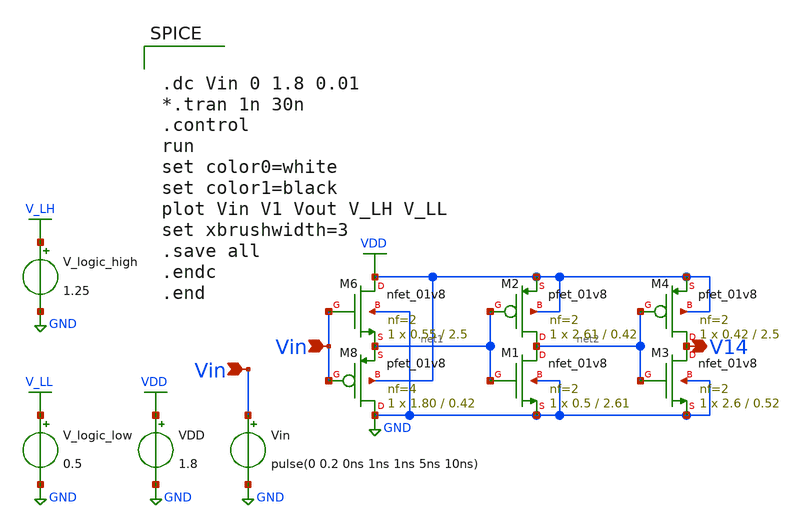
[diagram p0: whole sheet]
** sch_path: xschem/tr1/th14.sch
**.subckt th14 Vin Vin V14
*.ipin Vin
*.ipin Vin
*.opin V14
VDD VDD GND 1.8
Vin Vin GND pulse(0 0.2 0ns 1ns 1ns 5ns 10ns)
V_logic_high V_LH GND 1.25
V_logic_low V_LL GND 0.5
XM6 VDD Vin net1 GND sky130_fd_pr__nfet_01v8 L=2.5 W=0.55 nf=2 ad='int((nf+1)/2) * W/nf * 0.29' as='int((nf+2)/2) * W/nf * 0.29'
+ pd='2*int((nf+1)/2) * (W/nf + 0.29)' ps='2*int((nf+2)/2) * (W/nf + 0.29)' nrd='0.29 / W' nrs='0.29 / W'
+ sa=0 sb=0 sd=0 mult=1 m=1
XM8 GND Vin net1 VDD sky130_fd_pr__pfet_01v8 L=0.42 W=1.80 nf=4 ad='int((nf+1)/2) * W/nf * 0.29' as='int((nf+2)/2) * W/nf * 0.29'
+ pd='2*int((nf+1)/2) * (W/nf + 0.29)' ps='2*int((nf+2)/2) * (W/nf + 0.29)' nrd='0.29 / W' nrs='0.29 / W'
+ sa=0 sb=0 sd=0 mult=1 m=1
XM1 net2 net1 GND GND sky130_fd_pr__nfet_01v8 L=2.61 W=0.5 nf=2 ad='int((nf+1)/2) * W/nf * 0.29' as='int((nf+2)/2) * W/nf * 0.29'
+ pd='2*int((nf+1)/2) * (W/nf + 0.29)' ps='2*int((nf+2)/2) * (W/nf + 0.29)' nrd='0.29 / W' nrs='0.29 / W'
+ sa=0 sb=0 sd=0 mult=1 m=1
XM2 net2 net1 VDD VDD sky130_fd_pr__pfet_01v8 L=0.42 W=2.61 nf=2 ad='int((nf+1)/2) * W/nf * 0.29' as='int((nf+2)/2) * W/nf * 0.29'
+ pd='2*int((nf+1)/2) * (W/nf + 0.29)' ps='2*int((nf+2)/2) * (W/nf + 0.29)' nrd='0.29 / W' nrs='0.29 / W'
+ sa=0 sb=0 sd=0 mult=1 m=1
XM3 V14 net2 GND GND sky130_fd_pr__nfet_01v8 L=0.52 W=2.6 nf=2 ad='int((nf+1)/2) * W/nf * 0.29' as='int((nf+2)/2) * W/nf * 0.29'
+ pd='2*int((nf+1)/2) * (W/nf + 0.29)' ps='2*int((nf+2)/2) * (W/nf + 0.29)' nrd='0.29 / W' nrs='0.29 / W'
+ sa=0 sb=0 sd=0 mult=1 m=1
XM4 V14 net2 VDD VDD sky130_fd_pr__pfet_01v8 L=2.5 W=0.42 nf=2 ad='int((nf+1)/2) * W/nf * 0.29' as='int((nf+2)/2) * W/nf * 0.29'
+ pd='2*int((nf+1)/2) * (W/nf + 0.29)' ps='2*int((nf+2)/2) * (W/nf + 0.29)' nrd='0.29 / W' nrs='0.29 / W'
+ sa=0 sb=0 sd=0 mult=1 m=1
**** begin user architecture code


.lib /usr/local/share/pdk/sky130A/libs.tech/ngspice/sky130.lib.spice tt

.save all





.dc Vin 0 1.8 0.01
*.tran 1n 30n
.control
run
set color0=white
set color1=black
plot Vin V1 Vout V_LH V_LL
set xbrushwidth=3
.save all
.endc
.end


**** end user architecture code
**.ends
.GLOBAL VDD
.GLOBAL GND
.GLOBAL V_LH
.GLOBAL V_LL
.end
